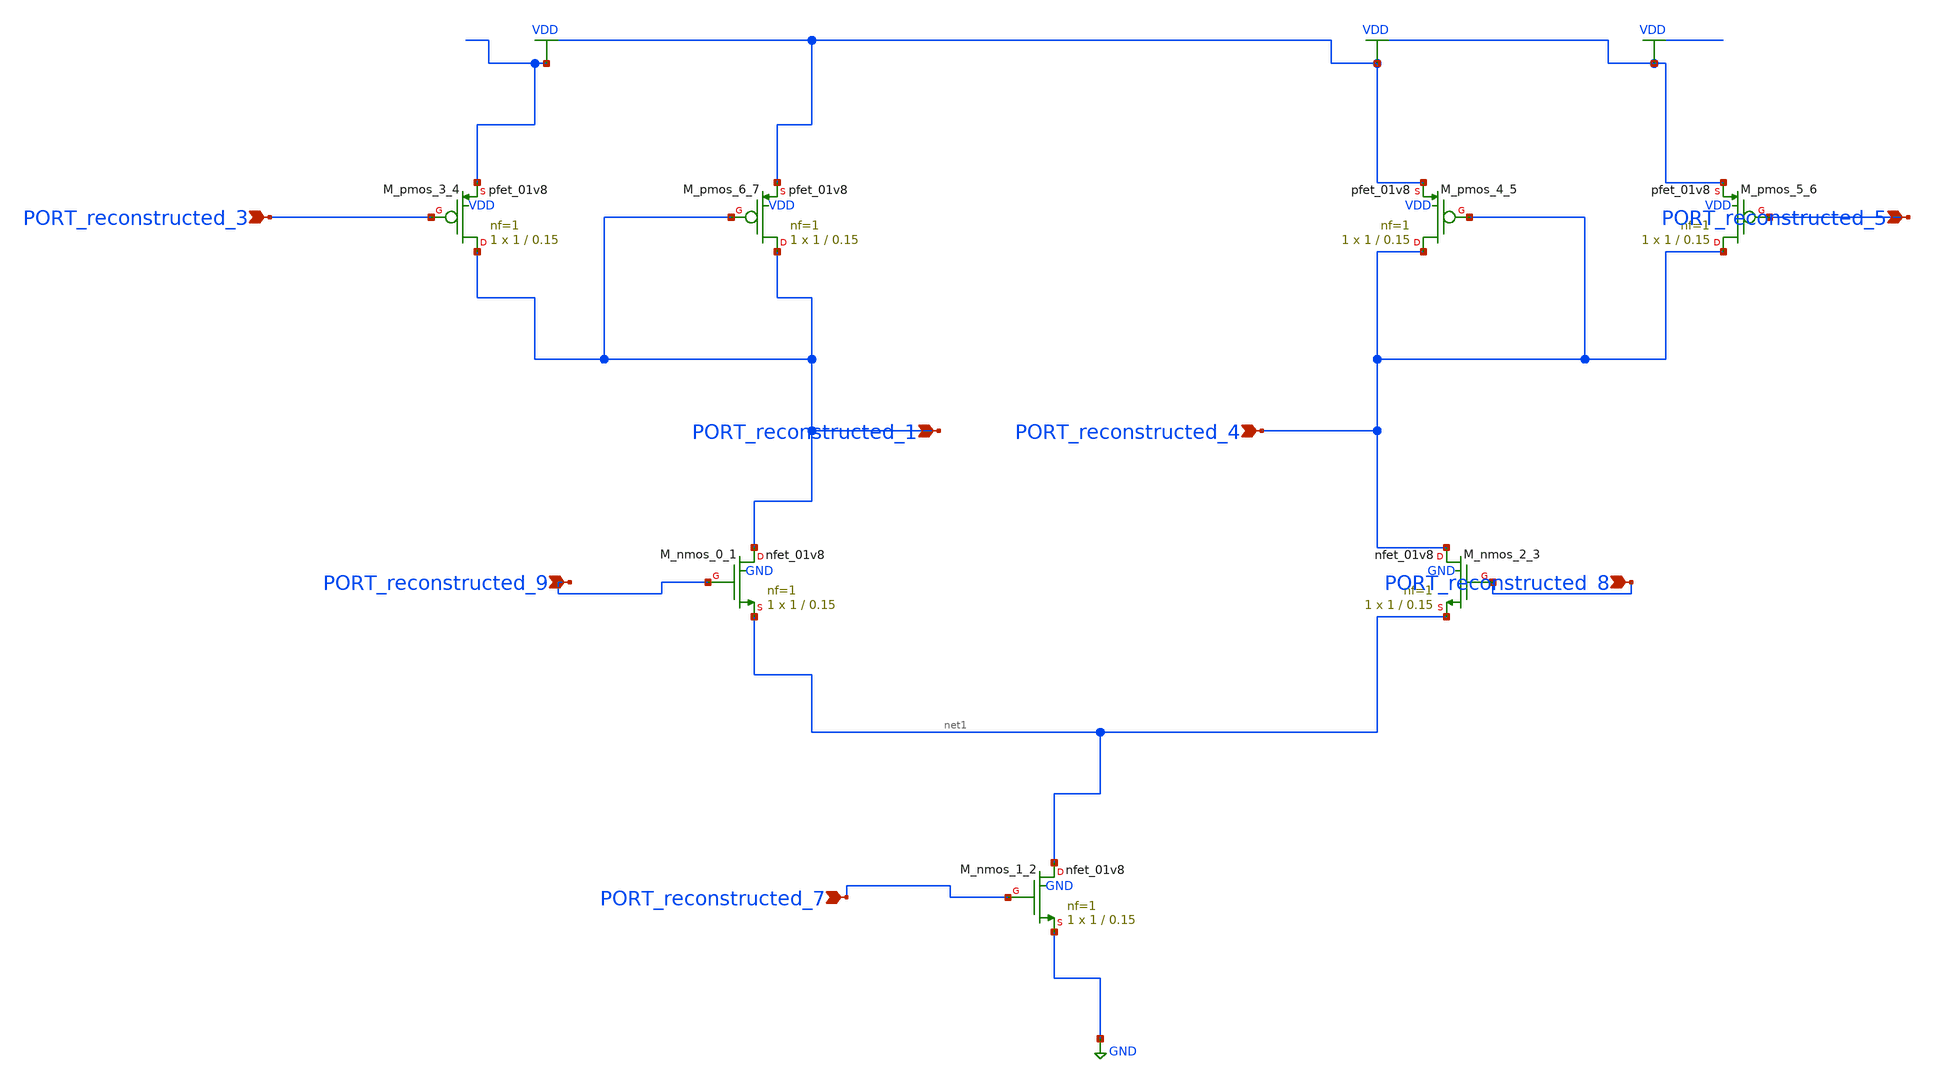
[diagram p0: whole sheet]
** sch_path: schematics/AMSNet/242.sch
**.subckt 242 PORT_reconstructed_7 PORT_reconstructed_8 PORT_reconstructed_4 PORT_reconstructed_5
*+ PORT_reconstructed_3 PORT_reconstructed_1 PORT_reconstructed_9
*.ipin PORT_reconstructed_7
*.ipin PORT_reconstructed_8
*.ipin PORT_reconstructed_4
*.ipin PORT_reconstructed_5
*.ipin PORT_reconstructed_3
*.ipin PORT_reconstructed_1
*.ipin PORT_reconstructed_9
XM_nmos_0_1 PORT_reconstructed_1 PORT_reconstructed_9 net1 GND sky130_fd_pr__nfet_01v8 L=0.15 W=1 nf=1
+ ad='int((1 + 1)/2) * 1 / 1 * 0.29' as='int((1 + 2)/2) * 1 / 1 * 0.29' pd='2*int((1 + 1)/2) * (1 / 1 + 0.29)'
+ ps='2*int((1 + 2)/2) * (1 / 1 + 0.29)' nrd='0.29 / 1 ' nrs='0.29 / 1 ' sa=0 sb=0 sd=0 mult=1 m=1
XM_nmos_1_2 net1 PORT_reconstructed_7 GND GND sky130_fd_pr__nfet_01v8 L=0.15 W=1 nf=1 ad='int((1 + 1)/2) * 1 / 1 * 0.29'
+ as='int((1 + 2)/2) * 1 / 1 * 0.29' pd='2*int((1 + 1)/2) * (1 / 1 + 0.29)' ps='2*int((1 + 2)/2) * (1 / 1 + 0.29)'
+ nrd='0.29 / 1 ' nrs='0.29 / 1 ' sa=0 sb=0 sd=0 mult=1 m=1
XM_nmos_2_3 PORT_reconstructed_4 PORT_reconstructed_8 net1 GND sky130_fd_pr__nfet_01v8 L=0.15 W=1 nf=1
+ ad='int((1 + 1)/2) * 1 / 1 * 0.29' as='int((1 + 2)/2) * 1 / 1 * 0.29' pd='2*int((1 + 1)/2) * (1 / 1 + 0.29)'
+ ps='2*int((1 + 2)/2) * (1 / 1 + 0.29)' nrd='0.29 / 1 ' nrs='0.29 / 1 ' sa=0 sb=0 sd=0 mult=1 m=1
XM_pmos_3_4 PORT_reconstructed_1 PORT_reconstructed_3 VDD VDD sky130_fd_pr__pfet_01v8 L=0.15 W=1 nf=1
+ ad='int((1 + 1)/2) * 1 / 1 * 0.29' as='int((1 + 2)/2) * 1 / 1 * 0.29' pd='2*int((1 + 1)/2) * (1 / 1 + 0.29)'
+ ps='2*int((1 + 2)/2) * (1 / 1 + 0.29)' nrd='0.29 / 1 ' nrs='0.29 / 1 ' sa=0 sb=0 sd=0 mult=1 m=1
XM_pmos_4_5 PORT_reconstructed_4 PORT_reconstructed_4 VDD VDD sky130_fd_pr__pfet_01v8 L=0.15 W=1 nf=1
+ ad='int((1 + 1)/2) * 1 / 1 * 0.29' as='int((1 + 2)/2) * 1 / 1 * 0.29' pd='2*int((1 + 1)/2) * (1 / 1 + 0.29)'
+ ps='2*int((1 + 2)/2) * (1 / 1 + 0.29)' nrd='0.29 / 1 ' nrs='0.29 / 1 ' sa=0 sb=0 sd=0 mult=1 m=1
XM_pmos_5_6 PORT_reconstructed_4 PORT_reconstructed_5 VDD VDD sky130_fd_pr__pfet_01v8 L=0.15 W=1 nf=1
+ ad='int((1 + 1)/2) * 1 / 1 * 0.29' as='int((1 + 2)/2) * 1 / 1 * 0.29' pd='2*int((1 + 1)/2) * (1 / 1 + 0.29)'
+ ps='2*int((1 + 2)/2) * (1 / 1 + 0.29)' nrd='0.29 / 1 ' nrs='0.29 / 1 ' sa=0 sb=0 sd=0 mult=1 m=1
XM_pmos_6_7 PORT_reconstructed_1 PORT_reconstructed_1 VDD VDD sky130_fd_pr__pfet_01v8 L=0.15 W=1 nf=1
+ ad='int((1 + 1)/2) * 1 / 1 * 0.29' as='int((1 + 2)/2) * 1 / 1 * 0.29' pd='2*int((1 + 1)/2) * (1 / 1 + 0.29)'
+ ps='2*int((1 + 2)/2) * (1 / 1 + 0.29)' nrd='0.29 / 1 ' nrs='0.29 / 1 ' sa=0 sb=0 sd=0 mult=1 m=1
**.ends
.GLOBAL GND
.GLOBAL VDD
.end
